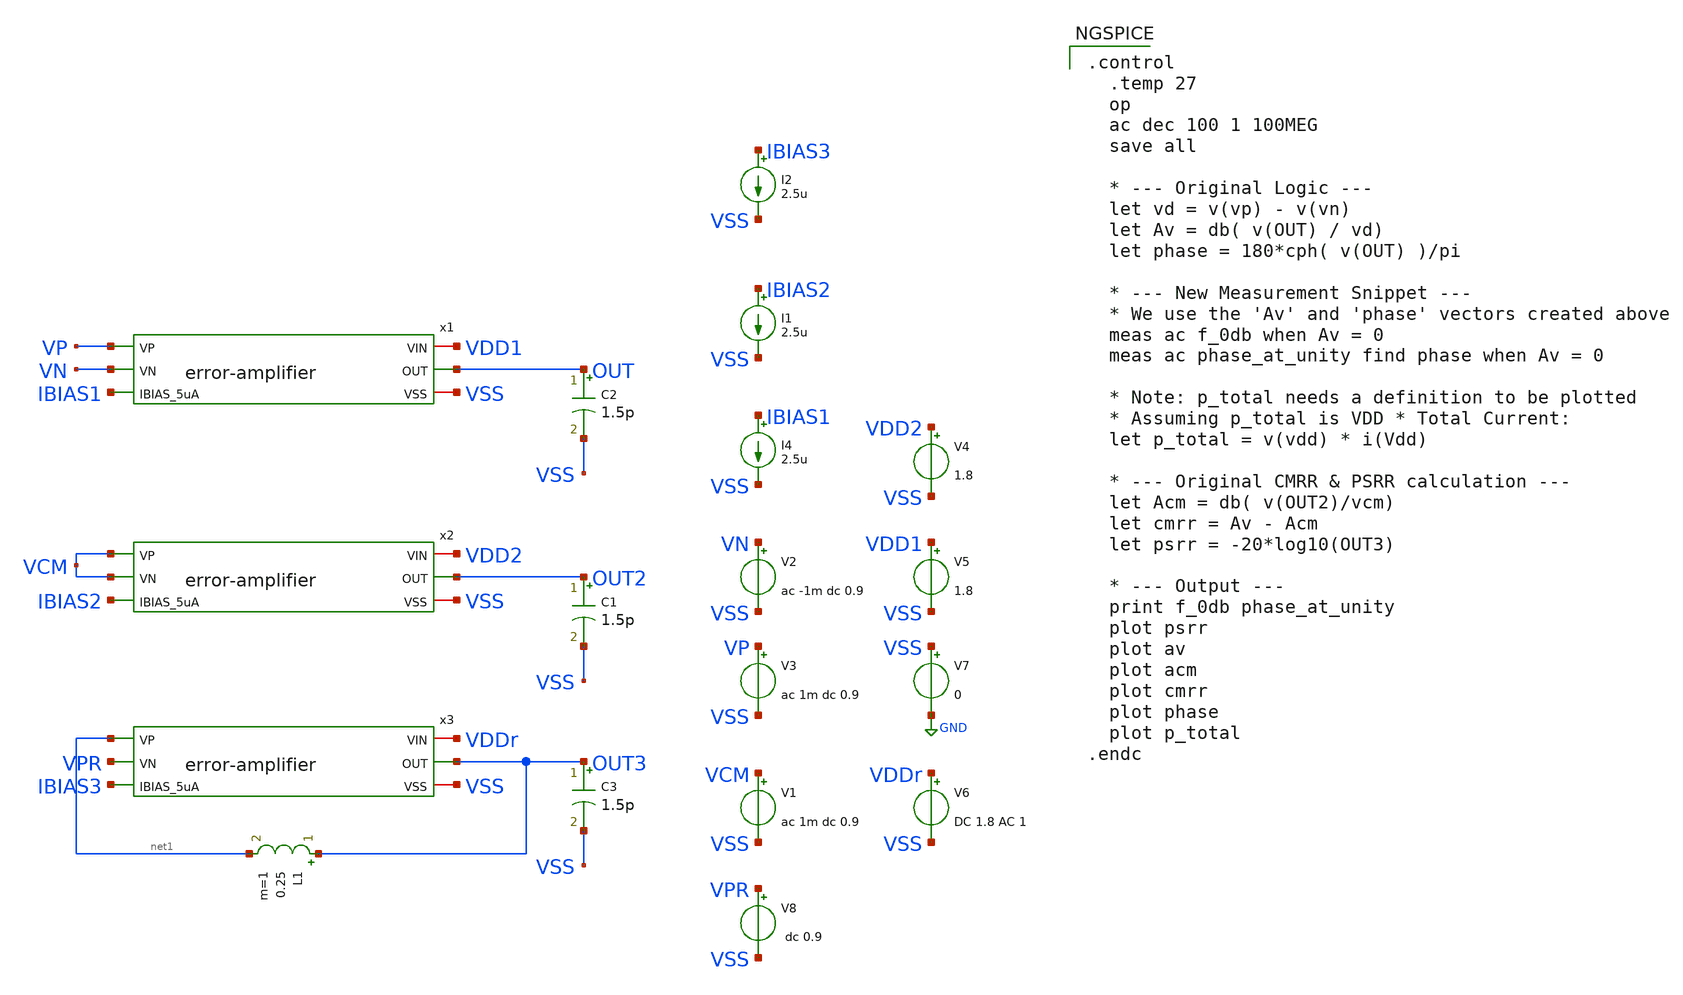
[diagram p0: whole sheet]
** sch_path: xschem/error-amplifier/testbench/tb_ac.sch
**.subckt tb_ac
V2 VN VSS ac -1m dc 0.9
V3 VP VSS ac 1m dc 0.9
V5 VDD1 VSS 1.8
V7 VSS GND 0
C2 OUT VSS 1.5p m=1
I4 IBIAS1 VSS 2.5u
C1 OUT2 VSS 1.5p m=1
V1 VCM VSS ac 1m dc 0.9
I1 IBIAS2 VSS 2.5u
V4 VDD2 VSS 1.8
C3 OUT3 VSS 1.5p m=1
V6 VDDr VSS DC 1.8 AC 1
L1 OUT3 net1 0.25 m=1
V8 VPR VSS dc 0.9
I2 IBIAS3 VSS 2.5u
x1 VDD1 VP VN IBIAS1 OUT VSS error-amplifier
x2 VDD2 VCM VCM IBIAS2 OUT2 VSS error-amplifier
x3 VDDr net1 VPR IBIAS3 OUT3 VSS error-amplifier
**** begin user architecture code

.control
  .temp 27
  op
  ac dec 100 1 100MEG
  save all

  * --- Original Logic ---
  let vd = v(vp) - v(vn)
  let Av = db( v(OUT) / vd)
  let phase = 180*cph( v(OUT) )/pi

  * --- New Measurement Snippet ---
  * We use the 'Av' and 'phase' vectors created above
  meas ac f_0db when Av = 0
  meas ac phase_at_unity find phase when Av = 0

  * Note: p_total needs a definition to be plotted
  * Assuming p_total is VDD * Total Current:
  let p_total = v(vdd) * i(Vdd)

  * --- Original CMRR & PSRR calculation ---
  let Acm = db( v(OUT2)/vcm)
  let cmrr = Av - Acm
  let psrr = -20*log10(OUT3)

  * --- Output ---
  print f_0db phase_at_unity
  plot psrr
  plot av
  plot acm
  plot cmrr
  plot phase
  plot p_total
.endc




** opencircuitdesign pdks install
.lib $::SKYWATER_MODELS/sky130.lib.spice ss


**** end user architecture code
**.ends

* expanding   symbol:
*+  /foss/designs/2026/tt_sky26b_ldo_andriansyah/xschem/error-amplifier/error-amplifier.sym # of pins=6
** sym_path: xschem/error-amplifier/error-amplifier.sym
** sch_path: xschem/error-amplifier/error-amplifier.sch
.subckt error-amplifier VIN VP VN IBIAS_5uA OUT VSS
*.ipin IBIAS_5uA
*.ipin VN
*.ipin VP
*.iopin VIN
*.iopin VSS
*.opin OUT
XM1 net2 net2 VSS VSS sky130_fd_pr__nfet_01v8 L=0.6 W=4.2 nf=4 ad='int((nf+1)/2) * W/nf * 0.29' as='int((nf+2)/2) * W/nf * 0.29'
+ pd='2*int((nf+1)/2) * (W/nf + 0.29)' ps='2*int((nf+2)/2) * (W/nf + 0.29)' nrd='0.29 / W' nrs='0.29 / W'
+ sa=0 sb=0 sd=0 mult=1 m=1
XM2 OUT net2 VSS VSS sky130_fd_pr__nfet_01v8 L=0.6 W=4.2 nf=4 ad='int((nf+1)/2) * W/nf * 0.29' as='int((nf+2)/2) * W/nf * 0.29'
+ pd='2*int((nf+1)/2) * (W/nf + 0.29)' ps='2*int((nf+2)/2) * (W/nf + 0.29)' nrd='0.29 / W' nrs='0.29 / W'
+ sa=0 sb=0 sd=0 mult=1 m=1
XM3 net2 VN net1 VDD sky130_fd_pr__pfet_01v8 L=0.6 W=28 nf=4 ad='int((nf+1)/2) * W/nf * 0.29' as='int((nf+2)/2) * W/nf * 0.29'
+ pd='2*int((nf+1)/2) * (W/nf + 0.29)' ps='2*int((nf+2)/2) * (W/nf + 0.29)' nrd='0.29 / W' nrs='0.29 / W'
+ sa=0 sb=0 sd=0 mult=1 m=1
XM4 OUT VP net1 VDD sky130_fd_pr__pfet_01v8 L=0.6 W=28 nf=4 ad='int((nf+1)/2) * W/nf * 0.29' as='int((nf+2)/2) * W/nf * 0.29'
+ pd='2*int((nf+1)/2) * (W/nf + 0.29)' ps='2*int((nf+2)/2) * (W/nf + 0.29)' nrd='0.29 / W' nrs='0.29 / W'
+ sa=0 sb=0 sd=0 mult=1 m=1
XM5 net1 IBIAS_5uA VIN VIN sky130_fd_pr__pfet_01v8 L=0.6 W=6.6 nf=4 ad='int((nf+1)/2) * W/nf * 0.29'
+ as='int((nf+2)/2) * W/nf * 0.29' pd='2*int((nf+1)/2) * (W/nf + 0.29)' ps='2*int((nf+2)/2) * (W/nf + 0.29)'
+ nrd='0.29 / W' nrs='0.29 / W' sa=0 sb=0 sd=0 mult=1 m=1
XM6 IBIAS_5uA IBIAS_5uA VIN VIN sky130_fd_pr__pfet_01v8 L=0.6 W=6.6 nf=4 ad='int((nf+1)/2) * W/nf * 0.29'
+ as='int((nf+2)/2) * W/nf * 0.29' pd='2*int((nf+1)/2) * (W/nf + 0.29)' ps='2*int((nf+2)/2) * (W/nf + 0.29)'
+ nrd='0.29 / W' nrs='0.29 / W' sa=0 sb=0 sd=0 mult=1 m=1
XM7 VDD VDD VDD VDD sky130_fd_pr__pfet_01v8 L=0.6 W=7 nf=1 ad='int((nf+1)/2) * W/nf * 0.29' as='int((nf+2)/2) * W/nf * 0.29'
+ pd='2*int((nf+1)/2) * (W/nf + 0.29)' ps='2*int((nf+2)/2) * (W/nf + 0.29)' nrd='0.29 / W' nrs='0.29 / W'
+ sa=0 sb=0 sd=0 mult=1 m=1
XM8 VSS VSS VSS VSS sky130_fd_pr__nfet_01v8 L=0.6 W=1.05 nf=1 ad='int((nf+1)/2) * W/nf * 0.29' as='int((nf+2)/2) * W/nf * 0.29'
+ pd='2*int((nf+1)/2) * (W/nf + 0.29)' ps='2*int((nf+2)/2) * (W/nf + 0.29)' nrd='0.29 / W' nrs='0.29 / W'
+ sa=0 sb=0 sd=0 mult=1 m=1
XM9 VDD VDD VDD VDD sky130_fd_pr__pfet_01v8 L=0.6 W=1.65 nf=1 ad='int((nf+1)/2) * W/nf * 0.29' as='int((nf+2)/2) * W/nf * 0.29'
+ pd='2*int((nf+1)/2) * (W/nf + 0.29)' ps='2*int((nf+2)/2) * (W/nf + 0.29)' nrd='0.29 / W' nrs='0.29 / W'
+ sa=0 sb=0 sd=0 mult=1 m=1
XM10 VSS VSS VSS VSS sky130_fd_pr__nfet_01v8 L=0.6 W=1.05 nf=1 ad='int((nf+1)/2) * W/nf * 0.29' as='int((nf+2)/2) * W/nf * 0.29'
+ pd='2*int((nf+1)/2) * (W/nf + 0.29)' ps='2*int((nf+2)/2) * (W/nf + 0.29)' nrd='0.29 / W' nrs='0.29 / W'
+ sa=0 sb=0 sd=0 mult=1 m=1
XM11 VDD VDD VDD VDD sky130_fd_pr__pfet_01v8 L=0.6 W=7 nf=1 ad='int((nf+1)/2) * W/nf * 0.29' as='int((nf+2)/2) * W/nf * 0.29'
+ pd='2*int((nf+1)/2) * (W/nf + 0.29)' ps='2*int((nf+2)/2) * (W/nf + 0.29)' nrd='0.29 / W' nrs='0.29 / W'
+ sa=0 sb=0 sd=0 mult=1 m=1
XM12 VDD VDD VDD VDD sky130_fd_pr__pfet_01v8 L=0.6 W=1.65 nf=1 ad='int((nf+1)/2) * W/nf * 0.29' as='int((nf+2)/2) * W/nf * 0.29'
+ pd='2*int((nf+1)/2) * (W/nf + 0.29)' ps='2*int((nf+2)/2) * (W/nf + 0.29)' nrd='0.29 / W' nrs='0.29 / W'
+ sa=0 sb=0 sd=0 mult=1 m=1
.ends

.GLOBAL GND
.end
